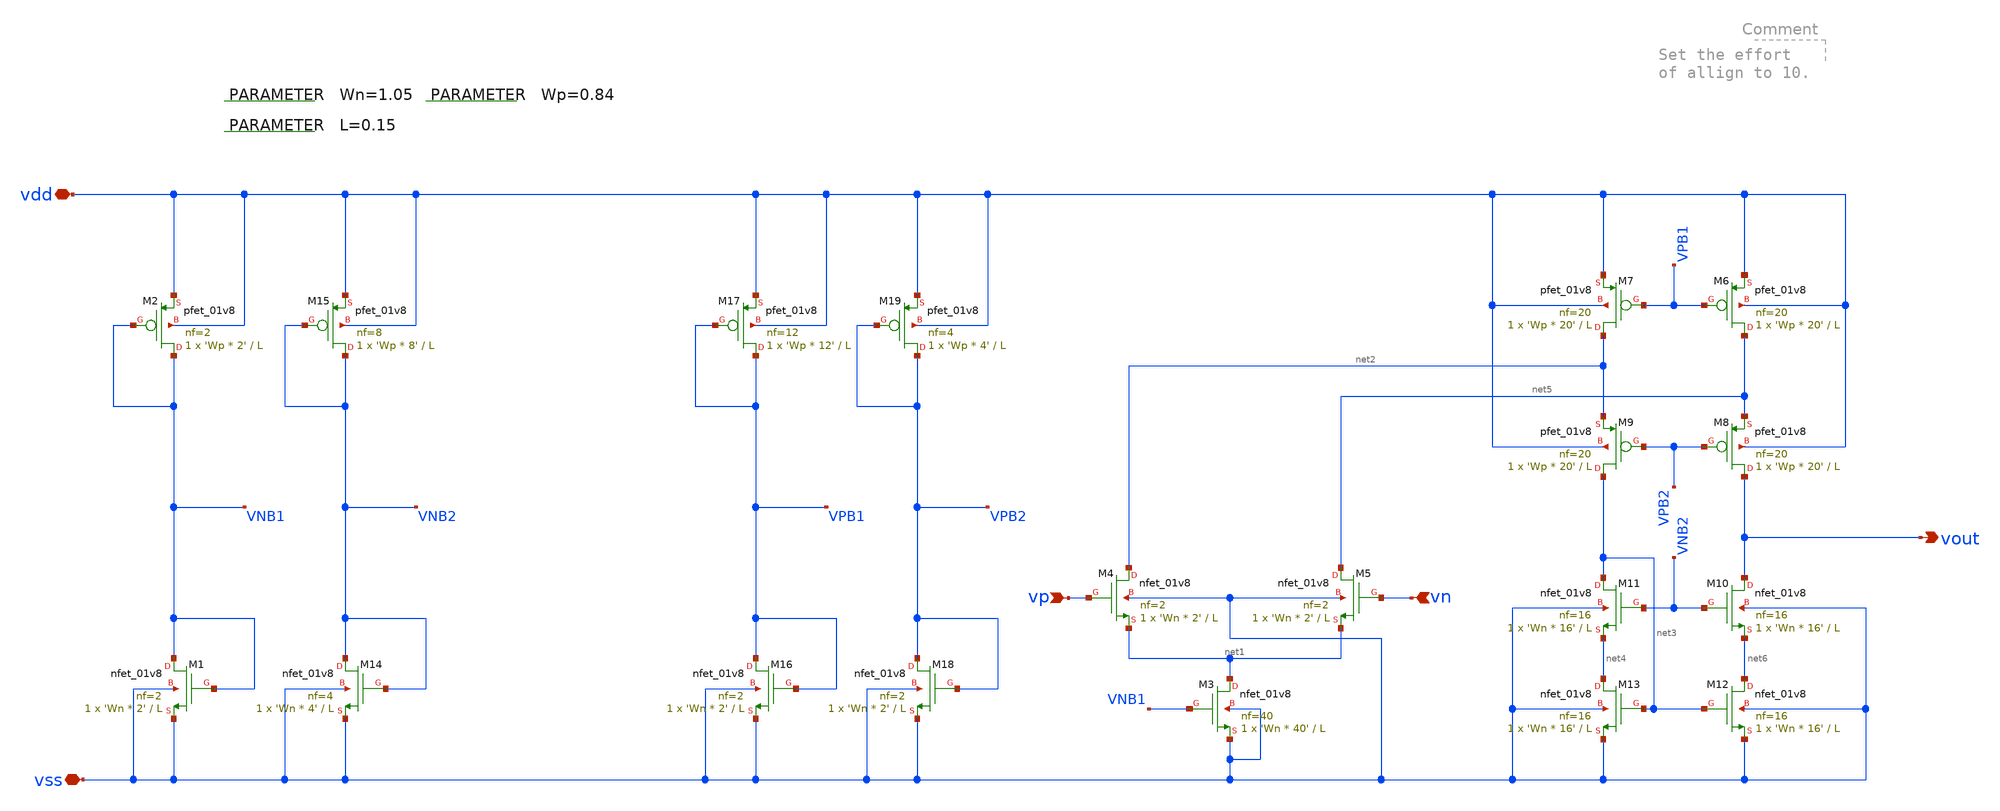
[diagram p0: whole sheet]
** sch_path: images/align/design/Examples/FoldedCascodeAmplifier/FoldedCascAmp.sch
**.subckt FoldedCascAmp vn vp vout vdd vss
*.ipin vn
*.ipin vp
*.opin vout
*.iopin vdd
*.iopin vss
.param Wn=1.05
.param L=0.15
.param Wp=0.84
XM1 VNB1 VNB1 vss vss sky130_fd_pr__nfet_01v8 L=L W='Wn * 2' nf=2 ad='int((nf+1)/2) * W/nf * 0.29' as='int((nf+2)/2) * W/nf * 0.29'
+ pd='2*int((nf+1)/2) * (W/nf + 0.29)' ps='2*int((nf+2)/2) * (W/nf + 0.29)' nrd='0.29 / W' nrs='0.29 / W'
+ sa=0 sb=0 sd=0 mult=1 m=1
XM2 VNB1 VNB1 vdd vdd sky130_fd_pr__pfet_01v8 L=L W='Wp * 2' nf=2 ad='int((nf+1)/2) * W/nf * 0.29' as='int((nf+2)/2) * W/nf * 0.29'
+ pd='2*int((nf+1)/2) * (W/nf + 0.29)' ps='2*int((nf+2)/2) * (W/nf + 0.29)' nrd='0.29 / W' nrs='0.29 / W'
+ sa=0 sb=0 sd=0 mult=1 m=1
XM3 net1 VNB1 vss vss sky130_fd_pr__nfet_01v8 L=L W='Wn * 40' nf=40 ad='int((nf+1)/2) * W/nf * 0.29'
+ as='int((nf+2)/2) * W/nf * 0.29' pd='2*int((nf+1)/2) * (W/nf + 0.29)' ps='2*int((nf+2)/2) * (W/nf + 0.29)'
+ nrd='0.29 / W' nrs='0.29 / W' sa=0 sb=0 sd=0 mult=1 m=1
XM4 net2 vp net1 vss sky130_fd_pr__nfet_01v8 L=L W='Wn * 2' nf=2 ad='int((nf+1)/2) * W/nf * 0.29' as='int((nf+2)/2) * W/nf * 0.29'
+ pd='2*int((nf+1)/2) * (W/nf + 0.29)' ps='2*int((nf+2)/2) * (W/nf + 0.29)' nrd='0.29 / W' nrs='0.29 / W'
+ sa=0 sb=0 sd=0 mult=1 m=1
XM5 net5 vn net1 vss sky130_fd_pr__nfet_01v8 L=L W='Wn * 2' nf=2 ad='int((nf+1)/2) * W/nf * 0.29' as='int((nf+2)/2) * W/nf * 0.29'
+ pd='2*int((nf+1)/2) * (W/nf + 0.29)' ps='2*int((nf+2)/2) * (W/nf + 0.29)' nrd='0.29 / W' nrs='0.29 / W'
+ sa=0 sb=0 sd=0 mult=1 m=1
XM6 net5 VPB1 vdd vdd sky130_fd_pr__pfet_01v8 L=L W='Wp * 20' nf=20 ad='int((nf+1)/2) * W/nf * 0.29'
+ as='int((nf+2)/2) * W/nf * 0.29' pd='2*int((nf+1)/2) * (W/nf + 0.29)' ps='2*int((nf+2)/2) * (W/nf + 0.29)'
+ nrd='0.29 / W' nrs='0.29 / W' sa=0 sb=0 sd=0 mult=1 m=1
XM7 net2 VPB1 vdd vdd sky130_fd_pr__pfet_01v8 L=L W='Wp * 20' nf=20 ad='int((nf+1)/2) * W/nf * 0.29'
+ as='int((nf+2)/2) * W/nf * 0.29' pd='2*int((nf+1)/2) * (W/nf + 0.29)' ps='2*int((nf+2)/2) * (W/nf + 0.29)'
+ nrd='0.29 / W' nrs='0.29 / W' sa=0 sb=0 sd=0 mult=1 m=1
XM8 vout VPB2 net5 vdd sky130_fd_pr__pfet_01v8 L=L W='Wp * 20' nf=20 ad='int((nf+1)/2) * W/nf * 0.29'
+ as='int((nf+2)/2) * W/nf * 0.29' pd='2*int((nf+1)/2) * (W/nf + 0.29)' ps='2*int((nf+2)/2) * (W/nf + 0.29)'
+ nrd='0.29 / W' nrs='0.29 / W' sa=0 sb=0 sd=0 mult=1 m=1
XM9 net3 VPB2 net2 vdd sky130_fd_pr__pfet_01v8 L=L W='Wp * 20' nf=20 ad='int((nf+1)/2) * W/nf * 0.29'
+ as='int((nf+2)/2) * W/nf * 0.29' pd='2*int((nf+1)/2) * (W/nf + 0.29)' ps='2*int((nf+2)/2) * (W/nf + 0.29)'
+ nrd='0.29 / W' nrs='0.29 / W' sa=0 sb=0 sd=0 mult=1 m=1
XM10 vout VNB2 net6 vss sky130_fd_pr__nfet_01v8 L=L W='Wn * 16' nf=16 ad='int((nf+1)/2) * W/nf * 0.29'
+ as='int((nf+2)/2) * W/nf * 0.29' pd='2*int((nf+1)/2) * (W/nf + 0.29)' ps='2*int((nf+2)/2) * (W/nf + 0.29)'
+ nrd='0.29 / W' nrs='0.29 / W' sa=0 sb=0 sd=0 mult=1 m=1
XM11 net3 VNB2 net4 vss sky130_fd_pr__nfet_01v8 L=L W='Wn * 16' nf=16 ad='int((nf+1)/2) * W/nf * 0.29'
+ as='int((nf+2)/2) * W/nf * 0.29' pd='2*int((nf+1)/2) * (W/nf + 0.29)' ps='2*int((nf+2)/2) * (W/nf + 0.29)'
+ nrd='0.29 / W' nrs='0.29 / W' sa=0 sb=0 sd=0 mult=1 m=1
XM12 net6 net3 vss vss sky130_fd_pr__nfet_01v8 L=L W='Wn * 16' nf=16 ad='int((nf+1)/2) * W/nf * 0.29'
+ as='int((nf+2)/2) * W/nf * 0.29' pd='2*int((nf+1)/2) * (W/nf + 0.29)' ps='2*int((nf+2)/2) * (W/nf + 0.29)'
+ nrd='0.29 / W' nrs='0.29 / W' sa=0 sb=0 sd=0 mult=1 m=1
XM13 net4 net3 vss vss sky130_fd_pr__nfet_01v8 L=L W='Wn * 16' nf=16 ad='int((nf+1)/2) * W/nf * 0.29'
+ as='int((nf+2)/2) * W/nf * 0.29' pd='2*int((nf+1)/2) * (W/nf + 0.29)' ps='2*int((nf+2)/2) * (W/nf + 0.29)'
+ nrd='0.29 / W' nrs='0.29 / W' sa=0 sb=0 sd=0 mult=1 m=1
XM14 VNB2 VNB2 vss vss sky130_fd_pr__nfet_01v8 L=L W='Wn * 4' nf=4 ad='int((nf+1)/2) * W/nf * 0.29' as='int((nf+2)/2) * W/nf * 0.29'
+ pd='2*int((nf+1)/2) * (W/nf + 0.29)' ps='2*int((nf+2)/2) * (W/nf + 0.29)' nrd='0.29 / W' nrs='0.29 / W'
+ sa=0 sb=0 sd=0 mult=1 m=1
XM15 VNB2 VNB2 vdd vdd sky130_fd_pr__pfet_01v8 L=L W='Wp * 8' nf=8 ad='int((nf+1)/2) * W/nf * 0.29' as='int((nf+2)/2) * W/nf * 0.29'
+ pd='2*int((nf+1)/2) * (W/nf + 0.29)' ps='2*int((nf+2)/2) * (W/nf + 0.29)' nrd='0.29 / W' nrs='0.29 / W'
+ sa=0 sb=0 sd=0 mult=1 m=1
XM16 VPB1 VPB1 vss vss sky130_fd_pr__nfet_01v8 L=L W='Wn * 2' nf=2 ad='int((nf+1)/2) * W/nf * 0.29' as='int((nf+2)/2) * W/nf * 0.29'
+ pd='2*int((nf+1)/2) * (W/nf + 0.29)' ps='2*int((nf+2)/2) * (W/nf + 0.29)' nrd='0.29 / W' nrs='0.29 / W'
+ sa=0 sb=0 sd=0 mult=1 m=1
XM17 VPB1 VPB1 vdd vdd sky130_fd_pr__pfet_01v8 L=L W='Wp * 12' nf=12 ad='int((nf+1)/2) * W/nf * 0.29'
+ as='int((nf+2)/2) * W/nf * 0.29' pd='2*int((nf+1)/2) * (W/nf + 0.29)' ps='2*int((nf+2)/2) * (W/nf + 0.29)'
+ nrd='0.29 / W' nrs='0.29 / W' sa=0 sb=0 sd=0 mult=1 m=1
XM18 VPB2 VPB2 vss vss sky130_fd_pr__nfet_01v8 L=L W='Wn * 2' nf=2 ad='int((nf+1)/2) * W/nf * 0.29' as='int((nf+2)/2) * W/nf * 0.29'
+ pd='2*int((nf+1)/2) * (W/nf + 0.29)' ps='2*int((nf+2)/2) * (W/nf + 0.29)' nrd='0.29 / W' nrs='0.29 / W'
+ sa=0 sb=0 sd=0 mult=1 m=1
XM19 VPB2 VPB2 vdd vdd sky130_fd_pr__pfet_01v8 L=L W='Wp * 4' nf=4 ad='int((nf+1)/2) * W/nf * 0.29' as='int((nf+2)/2) * W/nf * 0.29'
+ pd='2*int((nf+1)/2) * (W/nf + 0.29)' ps='2*int((nf+2)/2) * (W/nf + 0.29)' nrd='0.29 / W' nrs='0.29 / W'
+ sa=0 sb=0 sd=0 mult=1 m=1
**.ends
.end
